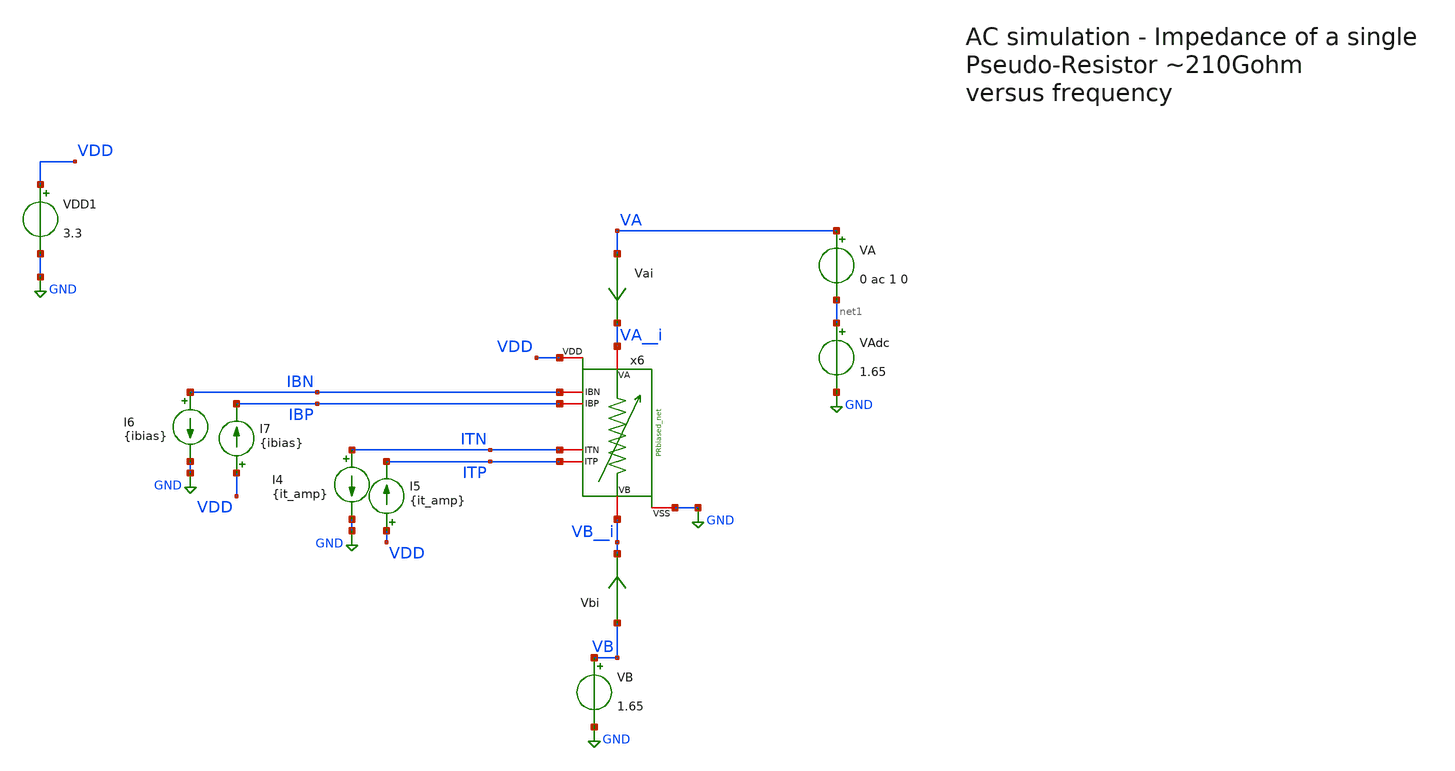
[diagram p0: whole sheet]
** sch_path: TIA_Filter/PseudoResistor/TB_PR_single_ac.sch
**.subckt TB_PR_single_ac
VDD1 VDD GND 3.3
VA VA net1 0 ac 1 0
VB VB GND 1.65
VAdc net1 GND 1.65
x6 VA__i VB__i IBN IBP ITN ITP VDD GND PRbiased_net
I4 ITN GND {it_amp}
I5 VDD ITP {it_amp}
I6 IBN GND {ibias}
I7 VDD IBP {ibias}
Vai VA VA__i 0
.save i(vai)
Vbi VB VB__i 0
.save i(vbi)
**** begin user architecture code

.include $::180MCU_MODELS/design.ngspice
.lib $::180MCU_MODELS/sm141064.ngspice typical

*.param sw_stat_mismatch=1
*.param sw_stat_global=1




.option savecurrents
.option gmin=1e-24

.param ibias = 1p
.param it_amp = 2p

.nodeset all=1.65

.control

  op
  let imped = 27
  save imped
  remzerovec
  write TB_PR_single_ac.raw
  set appendwrite

  set temp = 85
  ac dec 10 10m 1e5
  let imped = -V(va)/i(va)
  save imped
  remzerovec
  write TB_PR_single_ac.raw
  wrdata
+ /home/gmaranhao/Desktop/Bracolin/TIA_Filter/PseudoResistor/plots/data_DC/PR_single_AC_85.txt I(VA) imped

.endc
.save all


**** end user architecture code
**.ends
.GLOBAL GND
.end
